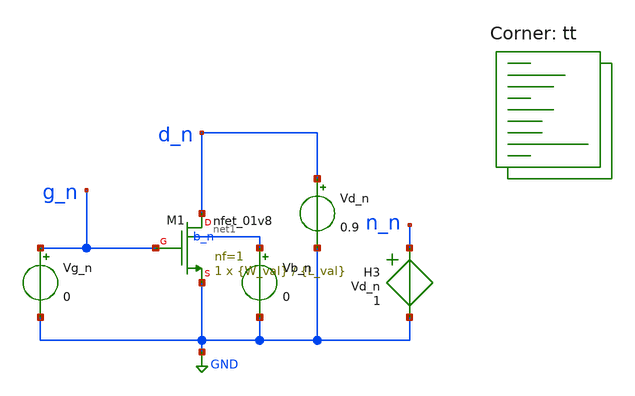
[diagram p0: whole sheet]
** sch_path: xschem/Testing_1.sch
**.subckt Testing_1
XM1 d_n g_n GND b_n sky130_fd_pr__nfet_01v8 L={L_val} W={W_val} nf=1 ad='int((1 + 1)/2) * {W_val} / 1 * 0.29'
+ as='int((1 + 2)/2) * {W_val} / 1 * 0.29' pd='2*int((1 + 1)/2) * ({W_val} / 1 + 0.29)' ps='2*int((1 + 2)/2) * ({W_val} / 1 + 0.29)'
+ nrd='0.29 / {W_val} ' nrs='0.29 / {W_val} ' sa=0 sb=0 sd=0 mult=1 m=1
H3 n_n GND Vd_n 1
Vg_n g_n GND 0
Vd_n d_n GND 0.9
Vb_n net1 GND 0
**** begin user architecture code


* gm/ID Characterization for Sky130 nfet_01v8
* Parameters
.param W_val = 10
.param L_val = 0.5
.dc Vg_n 0 1.8 0.01

.save all @m.xm1.msky130_fd_pr__nfet_01v8[id]
.save @m.xm1.msky130_fd_pr__nfet_01v8[vth]
.save @m.xm1.msky130_fd_pr__nfet_01v8[gm]
.save @m.xm1.msky130_fd_pr__nfet_01v8[cgg]
.save @m.xm1.msky130_fd_pr__nfet_01v8[w]
.save @m.xm1.msky130_fd_pr__nfet_01v8[l]
.save @m.xm1.msky130_fd_pr__nfet_01v8[gds]


.control

  * Direct Plotting in ngspice
  set xbrushwidth=2
 * set plot_vov = ' '
 * set plot_gm_id = ' '
 * set plot_id_W = ' '
 * set plot_gm_gmds = ' '
 * set plot_fT =' '

 foreach val 1.0 3.0 3.0
  run
  let W_n = @m.xm1.msky130_fd_pr__nfet_01v8[w]
  let L_n = @m.xm1.msky130_fd_pr__nfet_01v8[l]
  let g_m_n = @m.xm1.msky130_fd_pr__nfet_01v8[gm]
  let i_d_n = @m.xm1.msky130_fd_pr__nfet_01v8[id]
  let v_th_n = @m.xm1.msky130_fd_pr__nfet_01v8[vth]
  let c_gg_n =  @m.xm1.msky130_fd_pr__nfet_01v8[cgg]
  let g_ds_n =  @m.xm1.msky130_fd_pr__nfet_01v8[gds]


  let gm_id_n = 'g_m_n/i_d_n'
  let v_ov_n = 'v(g_n) - v_th_n'

  let w_T_n = 'g_m_n/c_gg_n'
  let f_T_n = 'w_T_n/('2*pi')'

  let gm_gmds_n = 'g_m_n/g_ds_n'

  let id_W_n = 'i_d_n/W_n'

  alterparam L_val = $val
  reset
 end
   print dc1.L_n dc2.L_n dc3.L_n
  *plot $plot_id_W vs $plot_gm_id ylog xlabel 'Current Eff S/A' ylabel 'A/W' title 'NMOS Id/W vs gm/Id'
  *plot $plot_gm_gmds vs $plot_gm_id xlabel 'Current Eff S/A' ylabel 'Intrinsic Gain' title 'NMOS gm/Id vs gm/gds'
  *plot $plot_fT vs $plot_gm_id xlabel 'Current Eff S/A' ylabel 'Transit Frequency GHz' title 'NMOS Id/W vs fT'
  *plot $plot_gm_id vs $plot_vov xlabel 'Overdrive Voltage V' ylabel 'Current Eff S/A' title 'NMOS gm/Id vs Vov'

  plot dc1.id_W_n vs dc1.gm_id_n dc2.id_W_n vs dc2.gm_id_n dc3.id_W_n vs dc3.gm_id_n  ylog xlabel 'Current Eff S/A'
+ ylabel 'A/W' title 'NMOS Id/W vs gm/Id'
  plot dc1.gm_gmds_n vs dc1.gm_id_n dc2.gm_gmds_n vs dc2.gm_id_n dc3.gm_gmds_n vs dc3.gm_id_n xlabel
+ 'Current Eff S/A' ylabel 'Intrinsic Gain' title 'NMOS gm/Id vs gm/gds'
  plot dc1.f_T_n vs dc1.gm_id_n dc2.f_T_n vs dc2.gm_id_n dc3.f_T_n vs dc3.gm_id_n xlabel 'Current Eff S/A'
+ ylabel 'Transit Frequency GHz' title 'NMOS Id/W vs fT'
  plot dc1.gm_id_n vs dc1.v_ov_n dc2.gm_id_n vs dc2.v_ov_n dc3.gm_id_n vs dc3.v_ov_n xlabel 'Overdrive Voltage V'
+ ylabel 'Current Eff S/A' title 'NMOS gm/Id vs Vov'
  plot dc1.gm_id_n dc2.gm_id_n dc3.gm_id_n xlabel 'Vgs' ylabel 'Current Eff S/A' title 'NMOS gm/Id vs Vgs'



.endc
.end

.lib $::SKYWATER_MODELS/sky130.lib.spice tt
**** end user architecture code
**.ends
.GLOBAL GND
.end
